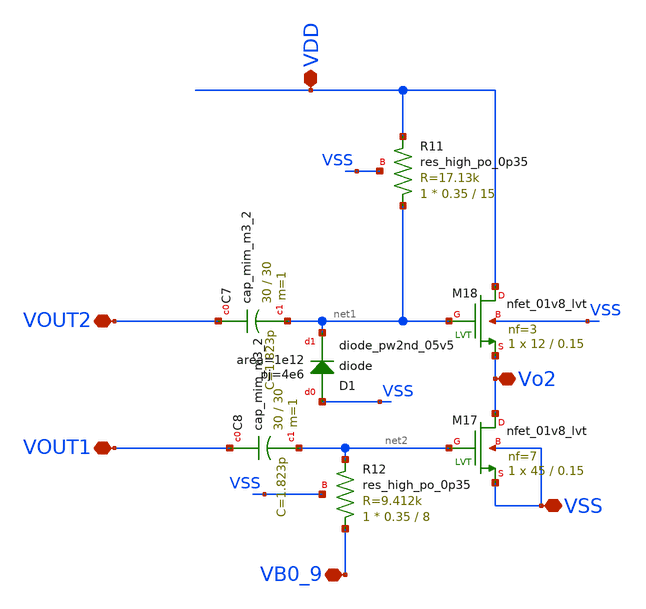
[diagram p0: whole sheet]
** sch_path: xschem/xschem4_sic_oct_20/partition3.sch
**.subckt partition3 VB0_9 VDD VSS VOUT2 VOUT1 Vo2
*.iopin VB0_9
*.iopin VDD
*.iopin VSS
*.iopin VOUT2
*.iopin VOUT1
*.iopin Vo2
XM17 Vo2 net2 VSS VSS sky130_fd_pr__nfet_01v8_lvt L=0.15 W=45 nf=7 ad='int((nf+1)/2) * W/nf * 0.29' as='int((nf+2)/2) * W/nf * 0.29'
+ pd='2*int((nf+1)/2) * (W/nf + 0.29)' ps='2*int((nf+2)/2) * (W/nf + 0.29)' nrd='0.29 / W' nrs='0.29 / W'
+ sa=0 sb=0 sd=0 mult=1 m=1
XM18 VDD net1 Vo2 VSS sky130_fd_pr__nfet_01v8_lvt L=0.15 W=12 nf=3 ad='int((nf+1)/2) * W/nf * 0.29' as='int((nf+2)/2) * W/nf * 0.29'
+ pd='2*int((nf+1)/2) * (W/nf + 0.29)' ps='2*int((nf+2)/2) * (W/nf + 0.29)' nrd='0.29 / W' nrs='0.29 / W'
+ sa=0 sb=0 sd=0 mult=1 m=1
XR11 net1 VDD VSS sky130_fd_pr__res_high_po_0p35 L=15 mult=1 m=1
XC7 VOUT2 net1 sky130_fd_pr__cap_mim_m3_2 W=30 L=30 MF=1 m=1
XR12 VB0_9 net2 VSS sky130_fd_pr__res_high_po_0p35 L=8 mult=1 m=1
XC8 VOUT1 net2 sky130_fd_pr__cap_mim_m3_2 W=30 L=30 MF=1 m=1
XD1 VSS net1 sky130_fd_pr__diode_pw2nd_05v5 area=1e12 pj=4e6
**.ends
.end
